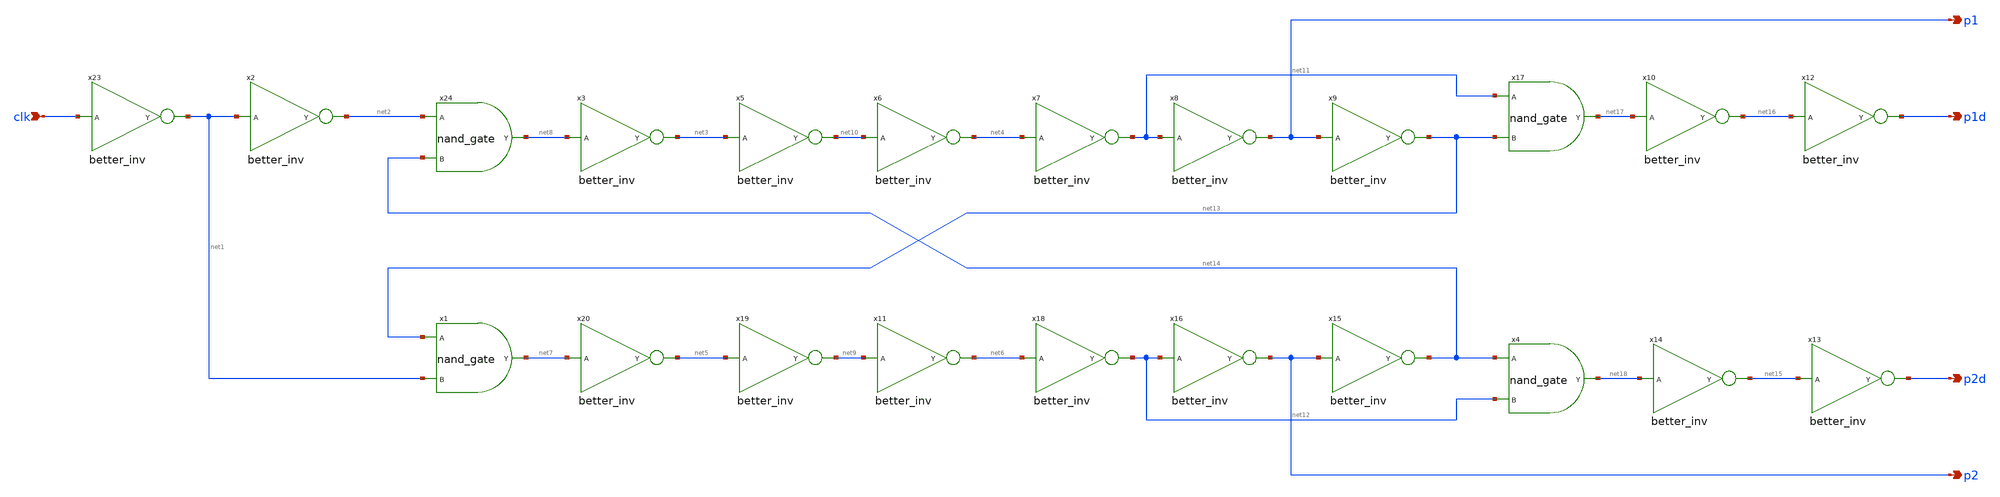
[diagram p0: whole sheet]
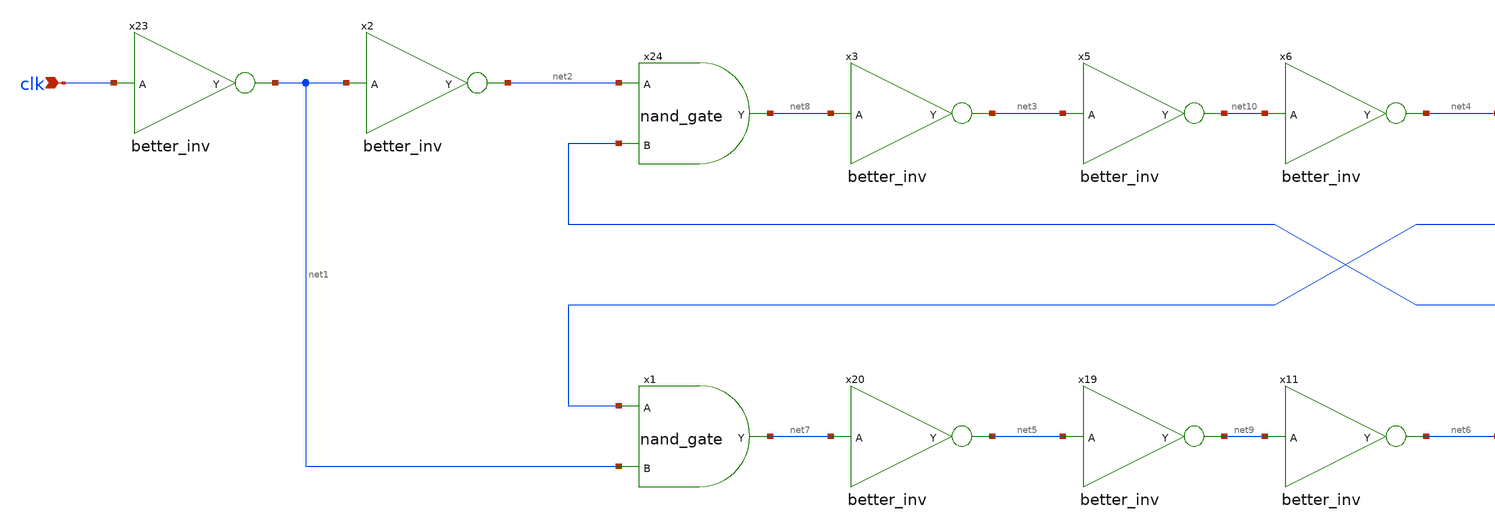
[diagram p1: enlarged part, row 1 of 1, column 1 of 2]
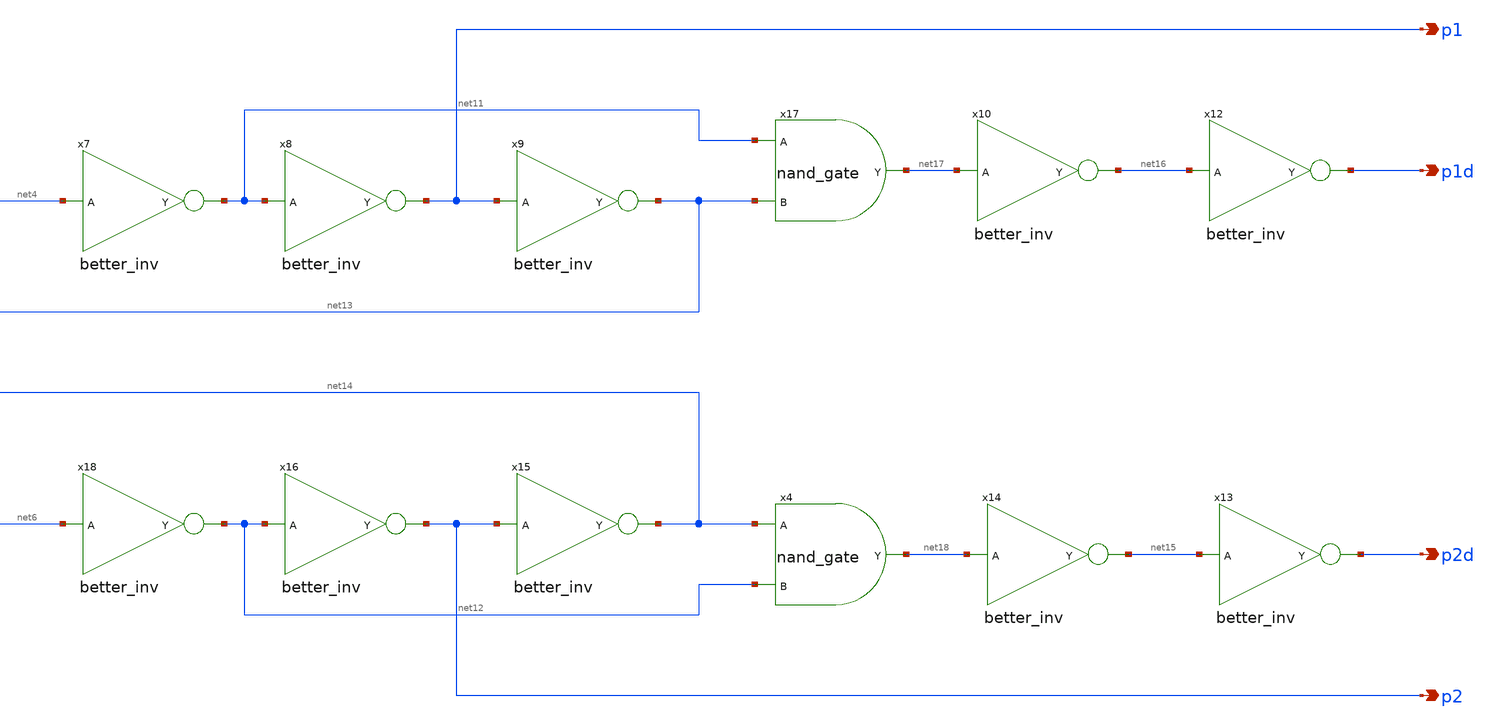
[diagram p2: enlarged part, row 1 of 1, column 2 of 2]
** sch_path: design/design_clkgen/clkgen.sch
**.subckt clkgen clk p1 p1d p2d p2
*.ipin clk
*.opin p1
*.opin p1d
*.opin p2d
*.opin p2
x11 net6 net9 better_inv
x23 net1 clk better_inv
x24 net8 net2 net14 nand_gate
x1 net7 net13 net1 nand_gate
x4 net18 net14 net12 nand_gate
x17 net17 net11 net13 nand_gate
x2 net2 net1 better_inv
x3 net3 net8 better_inv
x5 net10 net3 better_inv
x6 net4 net10 better_inv
x7 net11 net4 better_inv
x8 p1 net11 better_inv
x9 net13 p1 better_inv
x10 net16 net17 better_inv
x12 p1d net16 better_inv
x13 p2d net15 better_inv
x14 net15 net18 better_inv
x15 net14 p2 better_inv
x16 p2 net12 better_inv
x18 net12 net6 better_inv
x19 net9 net5 better_inv
x20 net5 net7 better_inv
**.ends
.end
